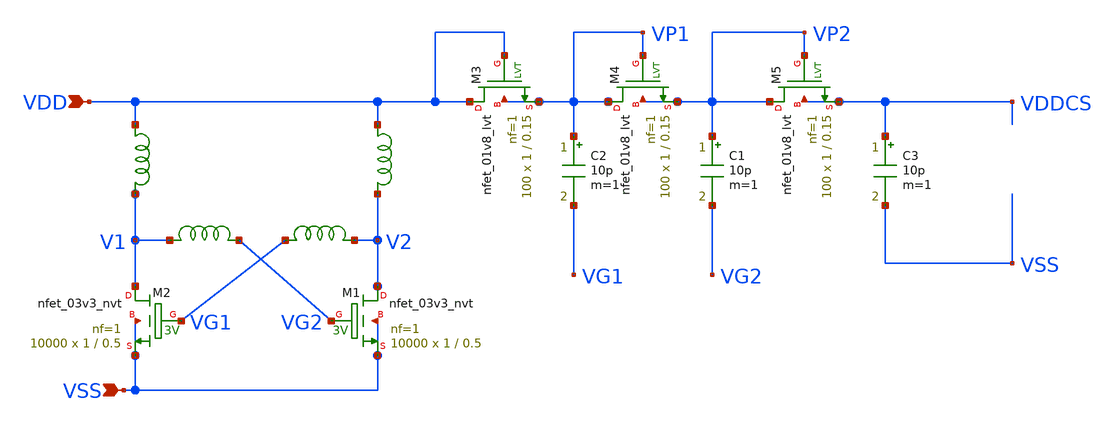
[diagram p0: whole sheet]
** sch_path: design/LELO_SVOD_SKY130A/LELO_EXSC.sch
**.subckt LELO_EXSC VSS VDD
*.ipin VSS
*.ipin VDD
C1 VP2 VG2 10p m=1
C2 VP1 VG1 10p m=1
XM2 V1 VG1 VSS VSS sky130_fd_pr__nfet_03v3_nvt L=0.5 W=1 nf=1 ad='int((1 + 1)/2) * 1 / 1 * 0.29' as='int((1 + 2)/2) * 1 / 1 * 0.29'
+ pd='2*int((1 + 1)/2) * (1 / 1 + 0.29)' ps='2*int((1 + 2)/2) * (1 / 1 + 0.29)' nrd='0.29 / 1 ' nrs='0.29 / 1 '
+ sa=0 sb=0 sd=0 mult=10000 m=10000
XM1 V2 VG2 VSS VSS sky130_fd_pr__nfet_03v3_nvt L=0.5 W=1 nf=1 ad='int((1 + 1)/2) * 1 / 1 * 0.29' as='int((1 + 2)/2) * 1 / 1 * 0.29'
+ pd='2*int((1 + 1)/2) * (1 / 1 + 0.29)' ps='2*int((1 + 2)/2) * (1 / 1 + 0.29)' nrd='0.29 / 1 ' nrs='0.29 / 1 '
+ sa=0 sb=0 sd=0 mult=10000 m=10000
x1 V1 VG2 1812PS-334_imp
x2 V2 VG1 1812PS-334_imp
x3 VDD V1 1812PS-102_imp
x4 VDD V2 1812PS-102_imp
C3 VDDCS VSS 10p m=1
XM3 VDD VDD VP1 VP1 sky130_fd_pr__nfet_01v8_lvt L=0.15 W=1 nf=1 ad='int((1 + 1)/2) * 1 / 1 * 0.29' as='int((1 + 2)/2) * 1 / 1 * 0.29'
+ pd='2*int((1 + 1)/2) * (1 / 1 + 0.29)' ps='2*int((1 + 2)/2) * (1 / 1 + 0.29)' nrd='0.29 / 1 ' nrs='0.29 / 1 '
+ sa=0 sb=0 sd=0 mult=100 m=100
XM4 VP1 VP1 VP2 VP2 sky130_fd_pr__nfet_01v8_lvt L=0.15 W=1 nf=1 ad='int((1 + 1)/2) * 1 / 1 * 0.29' as='int((1 + 2)/2) * 1 / 1 * 0.29'
+ pd='2*int((1 + 1)/2) * (1 / 1 + 0.29)' ps='2*int((1 + 2)/2) * (1 / 1 + 0.29)' nrd='0.29 / 1 ' nrs='0.29 / 1 '
+ sa=0 sb=0 sd=0 mult=100 m=100
XM5 VP2 VP2 VDDCS VDDCS sky130_fd_pr__nfet_01v8_lvt L=0.15 W=1 nf=1 ad='int((1 + 1)/2) * 1 / 1 * 0.29'
+ as='int((1 + 2)/2) * 1 / 1 * 0.29' pd='2*int((1 + 1)/2) * (1 / 1 + 0.29)' ps='2*int((1 + 2)/2) * (1 / 1 + 0.29)'
+ nrd='0.29 / 1 ' nrs='0.29 / 1 ' sa=0 sb=0 sd=0 mult=100 m=100
**.ends

* expanding   symbol:  LELO_SVOD_SKY130A/1812PS-334_imp.sym # of pins=2
** sym_path: design/LELO_SVOD_SKY130A/1812PS-334_imp.sym

.subckt 1812PS-334_imp port1 port2
X1 port1 port2 Model1D R1=75 R2=4.9 C= 2.43p K1=1E-06 K2=57.9 K3= 330u K4=0.000001 K5=0.000001 L=0
+ Is=0 a=0 L_Z0=0 L_EL=0 L_F0=0E6 PkZ=127597.141
.ends 1812PS-334_imp


* expanding   symbol:  LELO_SVOD_SKY130A/1812PS-102_imp.sym # of pins=2
** sym_path: design/LELO_SVOD_SKY130A/1812PS-102_imp.sym

.subckt 1812PS-102_imp port1 port2
X1 port1 port2 Model1D R1=60 R2=0.054 C= 0.15p K1=0.000001 K2=0.064 K3= 1u K4=1E-06 K5=0.000001 L=0
+ Is=0 a=0 L_Z0=0 L_EL=0 L_F0=0E6 PkZ=1282.46492
.ends 1812PS-102_imp
.end
